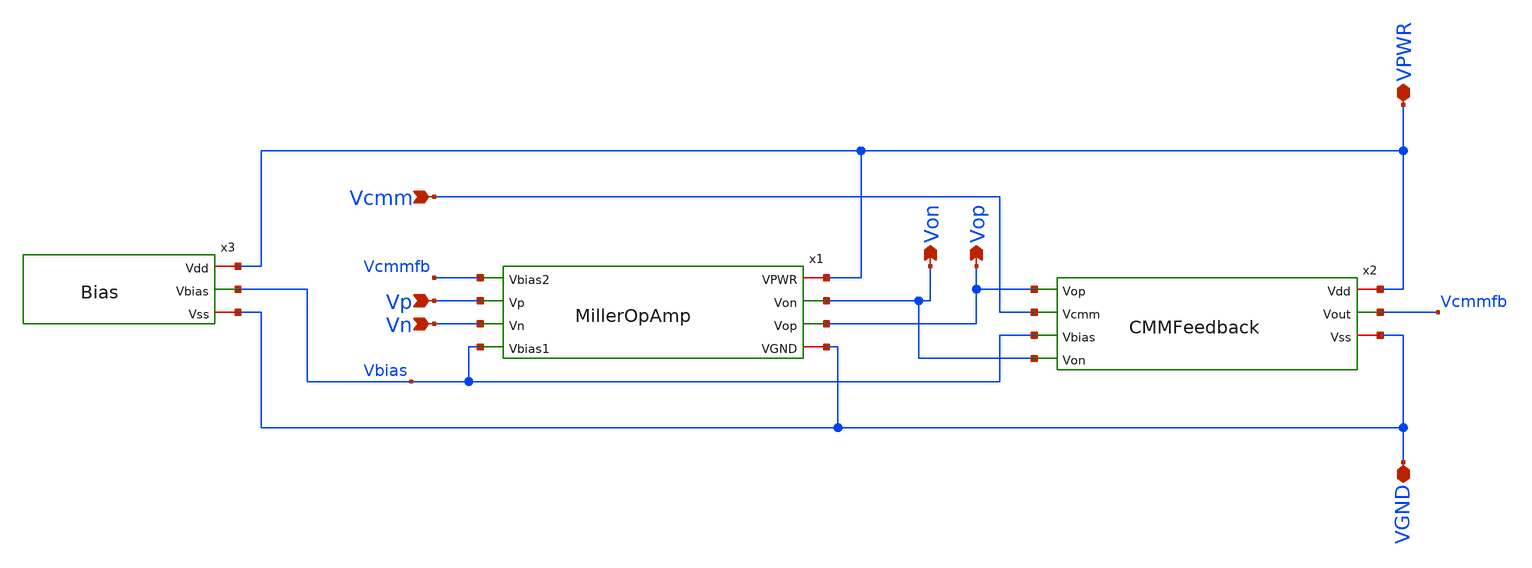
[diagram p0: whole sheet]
** sch_path: Circuits/MillerOpAmpCMMFB/OpAmp.sch
**.subckt OpAmp Von Vop Vcmm Vp Vn VPWR VGND
*.opin Von
*.opin Vop
*.ipin Vcmm
*.ipin Vp
*.ipin Vn
*.iopin VPWR
*.iopin VGND
x1 VPWR Von Vcmmfb Vp Vn Vbias Vop VGND MillerOpAmp
x2 Vop VPWR Vcmm Vcmmfb Vbias VGND Von CMMFeedback
x3 VPWR Vbias VGND Bias
**.ends
.end
